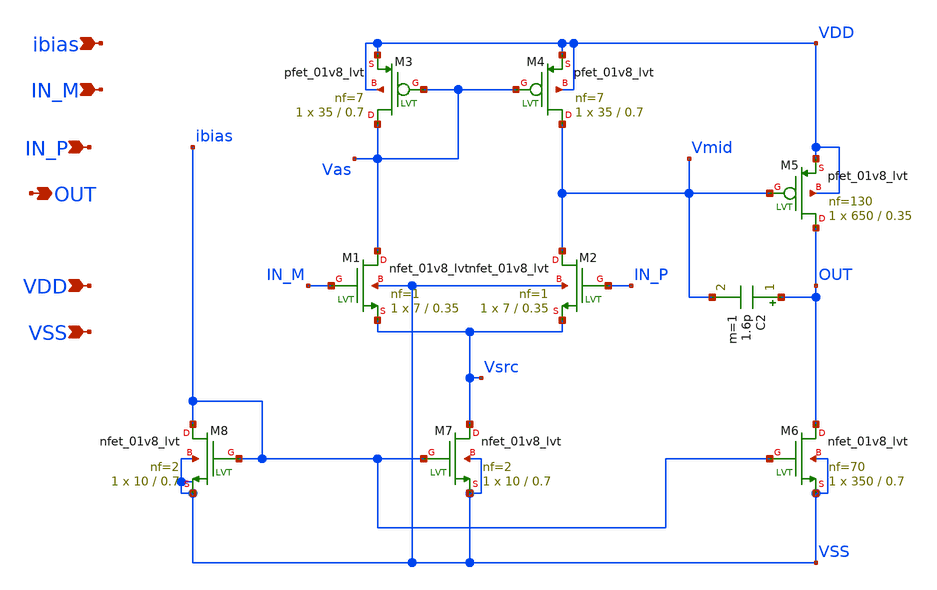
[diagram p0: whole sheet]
** sch_path: OTA_LASCAS2024.sch
**.subckt OTA_LASCAS2024 IN_M IN_P VDD VSS ibias OUT
*.ipin IN_M
*.ipin IN_P
*.ipin VDD
*.ipin VSS
*.ipin ibias
*.opin OUT
XM1 Vas IN_M Vsrc VSS sky130_fd_pr__nfet_01v8_lvt L=0.35 W=7 nf=1 ad='int((nf+1)/2) * W/nf * 0.29' as='int((nf+2)/2) * W/nf * 0.29'
+ pd='2*int((nf+1)/2) * (W/nf + 0.29)' ps='2*int((nf+2)/2) * (W/nf + 0.29)' nrd='0.29 / W' nrs='0.29 / W'
+ sa=0 sb=0 sd=0 mult=1 m=1
XM2 Vmid IN_P Vsrc VSS sky130_fd_pr__nfet_01v8_lvt L=0.35 W=7 nf=1 ad='int((nf+1)/2) * W/nf * 0.29' as='int((nf+2)/2) * W/nf * 0.29'
+ pd='2*int((nf+1)/2) * (W/nf + 0.29)' ps='2*int((nf+2)/2) * (W/nf + 0.29)' nrd='0.29 / W' nrs='0.29 / W'
+ sa=0 sb=0 sd=0 mult=1 m=1
XM3 Vas Vas VDD VDD sky130_fd_pr__pfet_01v8_lvt L=0.7 W=35 nf=7 ad='int((nf+1)/2) * W/nf * 0.29' as='int((nf+2)/2) * W/nf * 0.29'
+ pd='2*int((nf+1)/2) * (W/nf + 0.29)' ps='2*int((nf+2)/2) * (W/nf + 0.29)' nrd='0.29 / W' nrs='0.29 / W'
+ sa=0 sb=0 sd=0 mult=1 m=1
XM4 Vmid Vas VDD VDD sky130_fd_pr__pfet_01v8_lvt L=0.7 W=35 nf=7 ad='int((nf+1)/2) * W/nf * 0.29' as='int((nf+2)/2) * W/nf * 0.29'
+ pd='2*int((nf+1)/2) * (W/nf + 0.29)' ps='2*int((nf+2)/2) * (W/nf + 0.29)' nrd='0.29 / W' nrs='0.29 / W'
+ sa=0 sb=0 sd=0 mult=1 m=1
XM5 OUT Vmid VDD VDD sky130_fd_pr__pfet_01v8_lvt L=0.35 W=650 nf=130 ad='int((nf+1)/2) * W/nf * 0.29'
+ as='int((nf+2)/2) * W/nf * 0.29' pd='2*int((nf+1)/2) * (W/nf + 0.29)' ps='2*int((nf+2)/2) * (W/nf + 0.29)'
+ nrd='0.29 / W' nrs='0.29 / W' sa=0 sb=0 sd=0 mult=1 m=1
XM6 OUT ibias VSS VSS sky130_fd_pr__nfet_01v8_lvt L=0.7 W=350 nf=70 ad='int((nf+1)/2) * W/nf * 0.29'
+ as='int((nf+2)/2) * W/nf * 0.29' pd='2*int((nf+1)/2) * (W/nf + 0.29)' ps='2*int((nf+2)/2) * (W/nf + 0.29)'
+ nrd='0.29 / W' nrs='0.29 / W' sa=0 sb=0 sd=0 mult=1 m=1
XM7 Vsrc ibias VSS VSS sky130_fd_pr__nfet_01v8_lvt L=0.7 W=10 nf=2 ad='int((nf+1)/2) * W/nf * 0.29' as='int((nf+2)/2) * W/nf * 0.29'
+ pd='2*int((nf+1)/2) * (W/nf + 0.29)' ps='2*int((nf+2)/2) * (W/nf + 0.29)' nrd='0.29 / W' nrs='0.29 / W'
+ sa=0 sb=0 sd=0 mult=1 m=1
XM8 ibias ibias VSS VSS sky130_fd_pr__nfet_01v8_lvt L=0.7 W=10 nf=2 ad='int((nf+1)/2) * W/nf * 0.29'
+ as='int((nf+2)/2) * W/nf * 0.29' pd='2*int((nf+1)/2) * (W/nf + 0.29)' ps='2*int((nf+2)/2) * (W/nf + 0.29)'
+ nrd='0.29 / W' nrs='0.29 / W' sa=0 sb=0 sd=0 mult=1 m=1
C2 OUT Vmid 1.6p m=1
**.ends
.end
